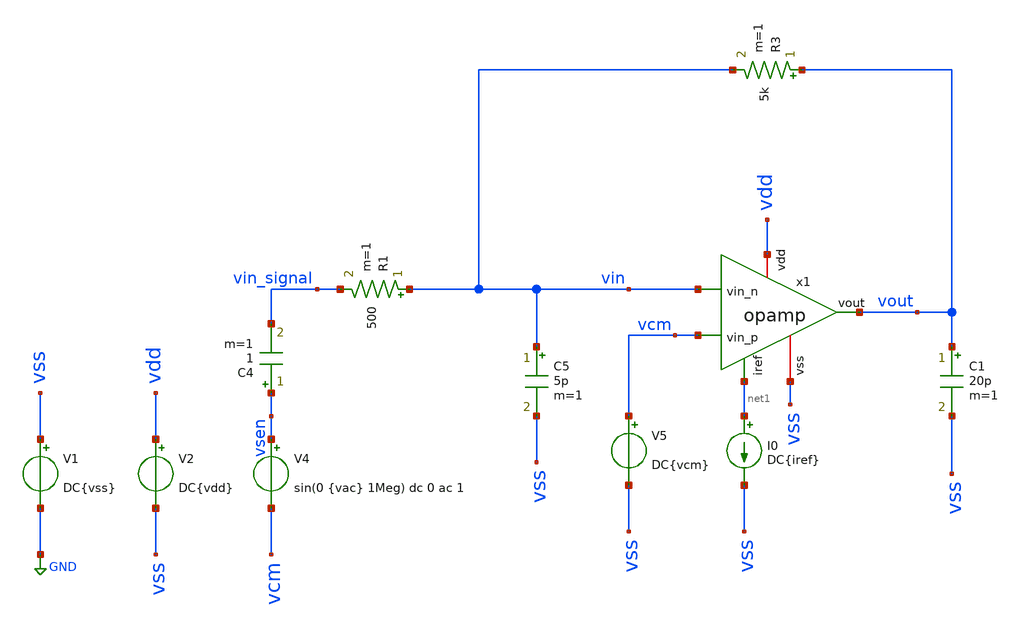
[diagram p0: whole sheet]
** sch_path: xsch/sch/opamp/opamp_closeloop.sch
**.subckt opamp_closeloop
V1 vss GND DC{vss}
V2 vdd vss DC{vdd}
V4 vsen vcm sin(0 {vac} 1Meg) dc 0 ac 1
C4 vsen vin_signal 1 m=1
I0 net1 vss DC{iref}
R1 vin vin_signal 500 m=1
R3 vout vin 5k m=1
C5 vin vss 5p m=1
x1 vdd net1 vin vcm vout vss opamp
C1 vout vss 20p m=1
V5 vcm vss DC{vcm}
**** begin user architecture code




* Circuit Parameters
.param iref = 100u
.param vdd  = 1.8
.param vss  = 0.0
.param vcm  = 0.8
.param vac  = 10m
.options TEMP = 65.0

* Include Models
.lib /home/tools/repos_sky130/skywater-pdk/libraries/sky130_fd_pr_ngspice/latest/models/corners/sky130.lib TT

* OP Parameters & Singals to save
.save all  @M.X1.XM1.msky130_fd_pr__pfet_01v8[id] @M.X1.XM1.msky130_fd_pr__pfet_01v8[vth] @M.X1.XM1.msky130_fd_pr__pfet_01v8[vgs] @M.X1.XM1.msky130_fd_pr__pfet_01v8[vds] @M.X1.XM1.msky130_fd_pr__pfet_01v8[vdsat] @M.X1.XM1.msky130_fd_pr__pfet_01v8[gm] @M.X1.XM1.msky130_fd_pr__pfet_01v8[gds]  @M.X1.XM2.msky130_fd_pr__pfet_01v8[id] @M.X1.XM2.msky130_fd_pr__pfet_01v8[vth] @M.X1.XM2.msky130_fd_pr__pfet_01v8[vgs] @M.X1.XM2.msky130_fd_pr__pfet_01v8[vds] @M.X1.XM2.msky130_fd_pr__pfet_01v8[vdsat] @M.X1.XM2.msky130_fd_pr__pfet_01v8[gm] @M.X1.XM2.msky130_fd_pr__pfet_01v8[gds]  @M.X1.XM3.msky130_fd_pr__nfet_01v8[id] @M.X1.XM3.msky130_fd_pr__nfet_01v8[vth] @M.X1.XM3.msky130_fd_pr__nfet_01v8[vgs] @M.X1.XM3.msky130_fd_pr__nfet_01v8[vds] @M.X1.XM3.msky130_fd_pr__nfet_01v8[vdsat] @M.X1.XM3.msky130_fd_pr__nfet_01v8[gm] @M.X1.XM3.msky130_fd_pr__nfet_01v8[gds]  @M.X1.XM4.msky130_fd_pr__nfet_01v8[id] @M.X1.XM4.msky130_fd_pr__nfet_01v8[vth] @M.X1.XM4.msky130_fd_pr__nfet_01v8[vgs] @M.X1.XM4.msky130_fd_pr__nfet_01v8[vds] @M.X1.XM4.msky130_fd_pr__nfet_01v8[vdsat] @M.X1.XM4.msky130_fd_pr__nfet_01v8[gm] @M.X1.XM4.msky130_fd_pr__nfet_01v8[gds]  @M.X1.XM5.msky130_fd_pr__pfet_01v8[id] @M.X1.XM5.msky130_fd_pr__pfet_01v8[vth] @M.X1.XM5.msky130_fd_pr__pfet_01v8[vgs] @M.X1.XM5.msky130_fd_pr__pfet_01v8[vds] @M.X1.XM5.msky130_fd_pr__pfet_01v8[vdsat] @M.X1.XM5.msky130_fd_pr__pfet_01v8[gm] @M.X1.XM5.msky130_fd_pr__pfet_01v8[gds]  @M.X1.XM6.msky130_fd_pr__nfet_01v8[id] @M.X1.XM6.msky130_fd_pr__nfet_01v8[vth] @M.X1.XM6.msky130_fd_pr__nfet_01v8[vgs] @M.X1.XM6.msky130_fd_pr__nfet_01v8[vds] @M.X1.XM6.msky130_fd_pr__nfet_01v8[vdsat] @M.X1.XM6.msky130_fd_pr__nfet_01v8[gm] @M.X1.XM6.msky130_fd_pr__nfet_01v8[gds]  @M.X1.XM7.msky130_fd_pr__pfet_01v8[id] @M.X1.XM7.msky130_fd_pr__pfet_01v8[vth] @M.X1.XM7.msky130_fd_pr__pfet_01v8[vgs] @M.X1.XM7.msky130_fd_pr__pfet_01v8[vds] @M.X1.XM7.msky130_fd_pr__pfet_01v8[vdsat] @M.X1.XM7.msky130_fd_pr__pfet_01v8[gm] @M.X1.XM7.msky130_fd_pr__pfet_01v8[gds]  @M.X1.XM8.msky130_fd_pr__pfet_01v8[id] @M.X1.XM8.msky130_fd_pr__pfet_01v8[vth] @M.X1.XM8.msky130_fd_pr__pfet_01v8[vgs] @M.X1.XM8.msky130_fd_pr__pfet_01v8[vds] @M.X1.XM8.msky130_fd_pr__pfet_01v8[vdsat] @M.X1.XM8.msky130_fd_pr__pfet_01v8[gm] @M.X1.XM8.msky130_fd_pr__pfet_01v8[gds]  @M.X1.XM9.msky130_fd_pr__nfet_01v8[id] @M.X1.XM9.msky130_fd_pr__nfet_01v8[vth] @M.X1.XM9.msky130_fd_pr__nfet_01v8[vgs] @M.X1.XM9.msky130_fd_pr__nfet_01v8[vds] @M.X1.XM9.msky130_fd_pr__nfet_01v8[vdsat] @M.X1.XM9.msky130_fd_pr__nfet_01v8[gm] @M.X1.XM9.msky130_fd_pr__nfet_01v8[gds]

*Simulations
.control
  ac dec 100 1k 10G
  setplot ac1
  meas ac GBW when vdb(vout)=0
  meas ac DCG find vdb(vout) at=1k
  *meas ac PM find vp(vout) when vdb(vout)=0
  *print PM*180/PI
  *meas ac GM find vdb(vout) when vp(vout)=0
  plot vdb(vout) {vp(vout)*180/PI}
  write ~/caravel_fulgor_opamp/xschem/opamp_diego/sim_results/opamp_closeloop_ac1.raw

  reset
  tran 0.01u 11u
  setplot tran1
  plot v(vsen) v(vout)
  write ~/caravel_fulgor_opamp/xschem/opamp_diego/sim_results/opamp_closeloop_tran1.raw

  reset
  noise v(vout) V4 dec 100 1k 10G 1
  setplot noise1
  plot inoise_spectrum onoise_spectrum
  *print inoise_spectrum
  *print onoise_spectrum
  setplot noise2
  *plot inoise_total onoise_total
  print inoise_total
  print onoise_total
  write ~/caravel_fulgor_opamp/xschem/opamp_diego/sim_results/opamp_closeloop_noise.raw

  reset
  op
  setplot op1
  print vout
  write ~/caravel_fulgor_opamp/xschem/opamp_diego/sim_results/opamp_closeloop_op1.raw

.endc

.end


**** end user architecture code
**.ends

* expanding   symbol:  opamp.sym # of pins=6
** sym_path: opamp.sym
** sch_path: opamp.sch
.subckt opamp vdd iref vin_n vin_p vout vss
*.iopin vdd
*.iopin vss
*.ipin vin_n
*.ipin vin_p
*.ipin iref
*.opin vout
XM1 vbn vin_n vp vp sky130_fd_pr__pfet_01v8 L=0.3 W=3 nf=1 ad='W * 0.29' as='W * 0.29' pd='2 * (W + 0.29)'
+ ps='2 * (W + 0.29)' nrd='0.29 / W' nrs='0.29 / W' sa=0 sb=0 sd=0 mult=200 m=200
XM2 voe1 vin_p vp vp sky130_fd_pr__pfet_01v8 L=0.3 W=3 nf=1 ad='W * 0.29' as='W * 0.29' pd='2 * (W + 0.29)'
+ ps='2 * (W + 0.29)' nrd='0.29 / W' nrs='0.29 / W' sa=0 sb=0 sd=0 mult=200 m=200
XM3 vbn vbn vss vss sky130_fd_pr__nfet_01v8 L=0.3 W=3 nf=1 ad='W * 0.29' as='W * 0.29' pd='2 * (W + 0.29)'
+ ps='2 * (W + 0.29)' nrd='0.29 / W' nrs='0.29 / W' sa=0 sb=0 sd=0 mult=30 m=30
XM4 voe1 vbn vss vss sky130_fd_pr__nfet_01v8 L=0.3 W=3 nf=1 ad='W * 0.29' as='W * 0.29' pd='2 * (W + 0.29)'
+ ps='2 * (W + 0.29)' nrd='0.29 / W' nrs='0.29 / W' sa=0 sb=0 sd=0 mult=30 m=30
XM5 vp iref vdd vdd sky130_fd_pr__pfet_01v8 L=0.3 W=3 nf=1 ad='W * 0.29' as='W * 0.29' pd='2 * (W + 0.29)'
+ ps='2 * (W + 0.29)' nrd='0.29 / W' nrs='0.29 / W' sa=0 sb=0 sd=0 mult=30 m=30
XM7 vout iref vdd vdd sky130_fd_pr__pfet_01v8 L=0.3 W=3 nf=1 ad='W * 0.29' as='W * 0.29' pd='2 * (W + 0.29)'
+ ps='2 * (W + 0.29)' nrd='0.29 / W' nrs='0.29 / W' sa=0 sb=0 sd=0 mult=150 m=150
XM8 iref iref vdd vdd sky130_fd_pr__pfet_01v8 L=0.3 W=3 nf=1 ad='W * 0.29' as='W * 0.29' pd='2 * (W + 0.29)'
+ ps='2 * (W + 0.29)' nrd='0.29 / W' nrs='0.29 / W' sa=0 sb=0 sd=0 mult=15 m=15
XM9 net1 vdd voe1 vss sky130_fd_pr__nfet_01v8 L=0.15 W=0.75 nf=1 ad='W * 0.29' as='W * 0.29' pd='2 * (W + 0.29)'
+ ps='2 * (W + 0.29)' nrd='0.29 / W' nrs='0.29 / W' sa=0 sb=0 sd=0 mult=6 m=6
XC1 net1 vout sky130_fd_pr__cap_mim_m3_1 W=17.55 L=15 MF=6 m=6
XM6 vout voe1 vss vss sky130_fd_pr__nfet_01v8 L=0.45 W=4.5 nf=1 ad='W * 0.29' as='W * 0.29' pd='2 * (W + 0.29)'
+ ps='2 * (W + 0.29)' nrd='0.29 / W' nrs='0.29 / W' sa=0 sb=0 sd=0 mult=150 m=150
.ends

.GLOBAL GND
.end
